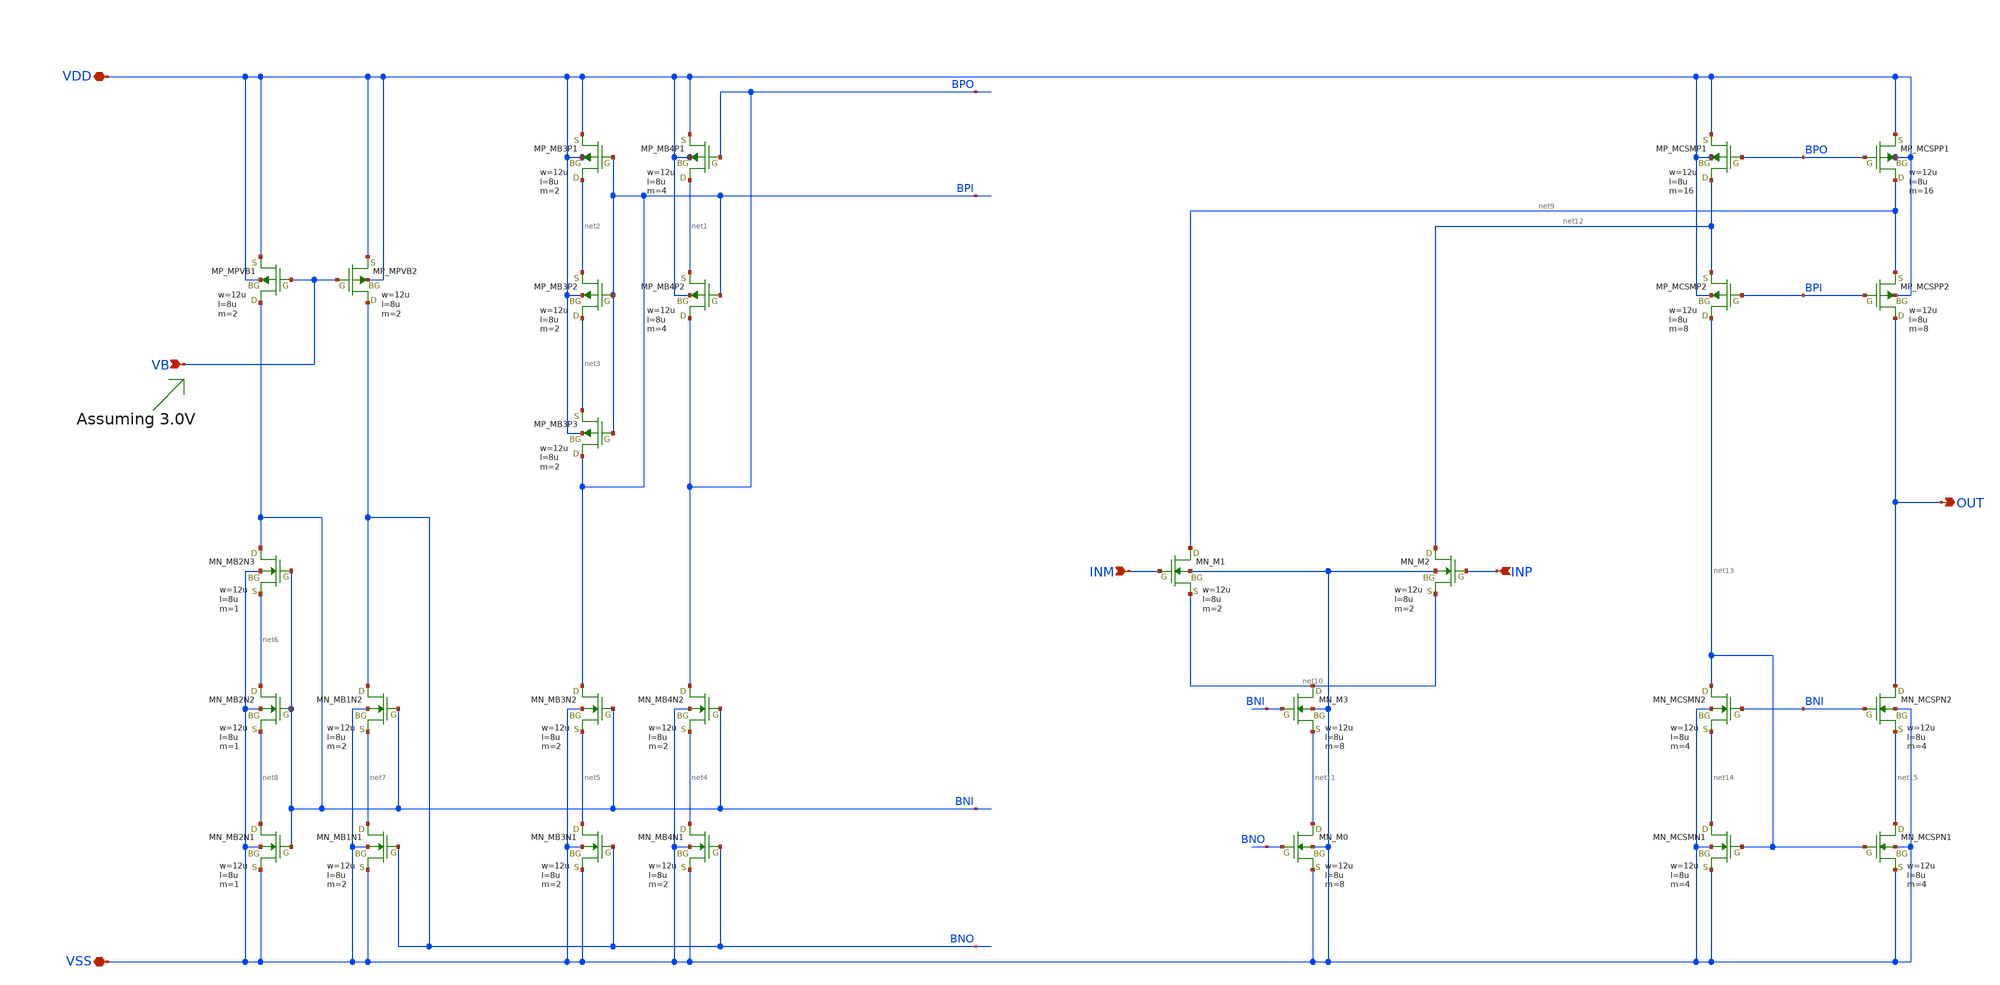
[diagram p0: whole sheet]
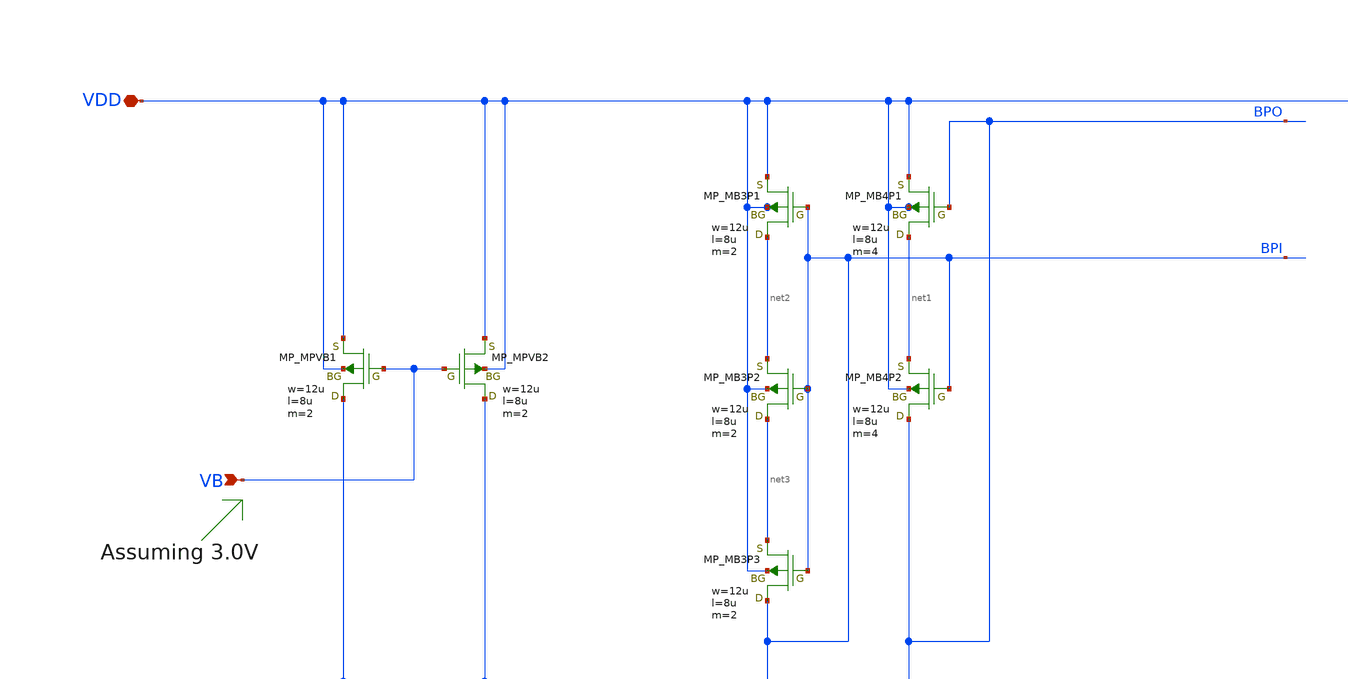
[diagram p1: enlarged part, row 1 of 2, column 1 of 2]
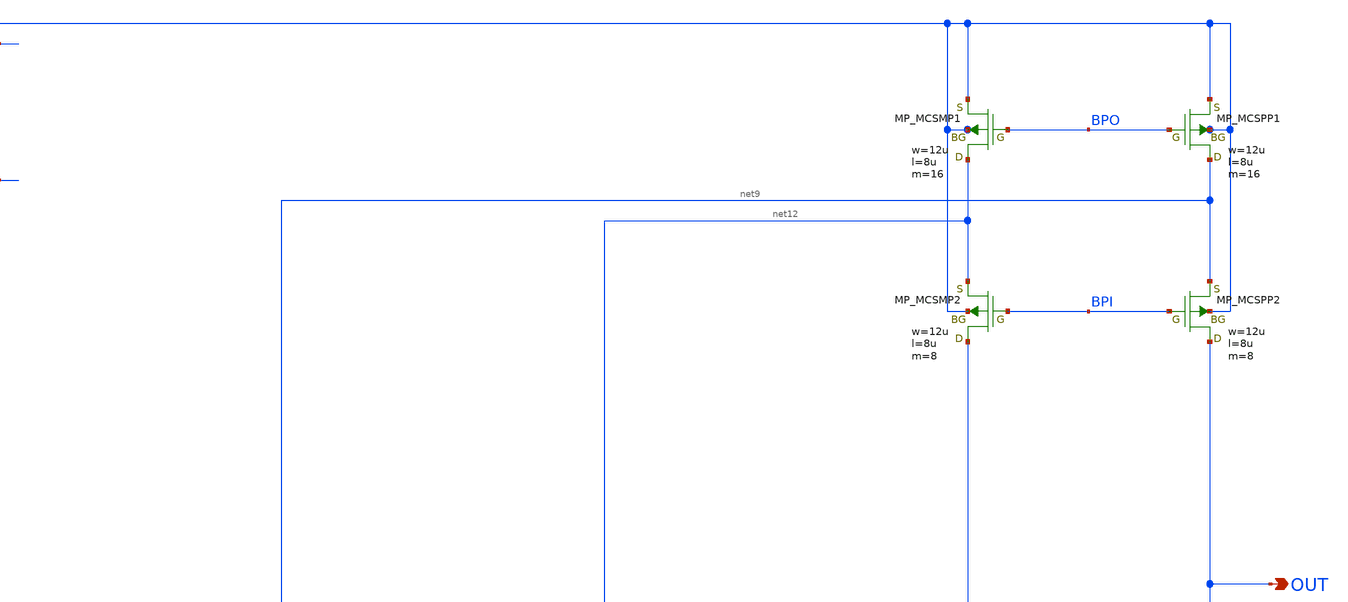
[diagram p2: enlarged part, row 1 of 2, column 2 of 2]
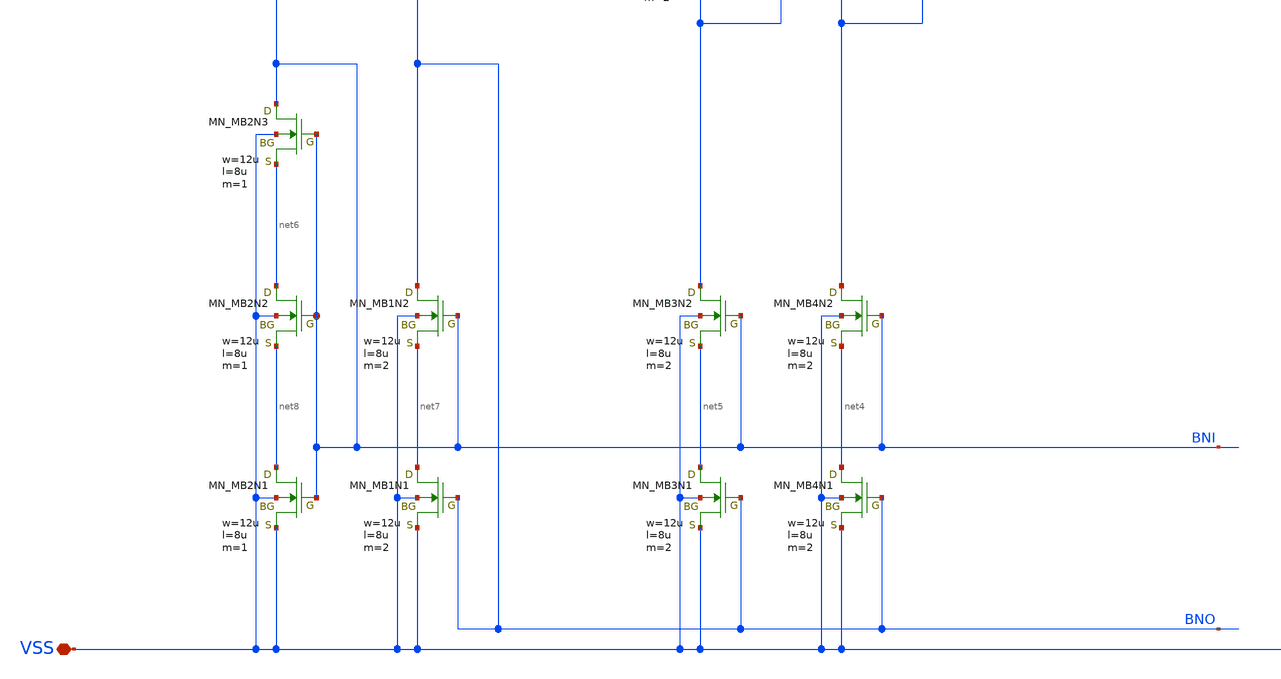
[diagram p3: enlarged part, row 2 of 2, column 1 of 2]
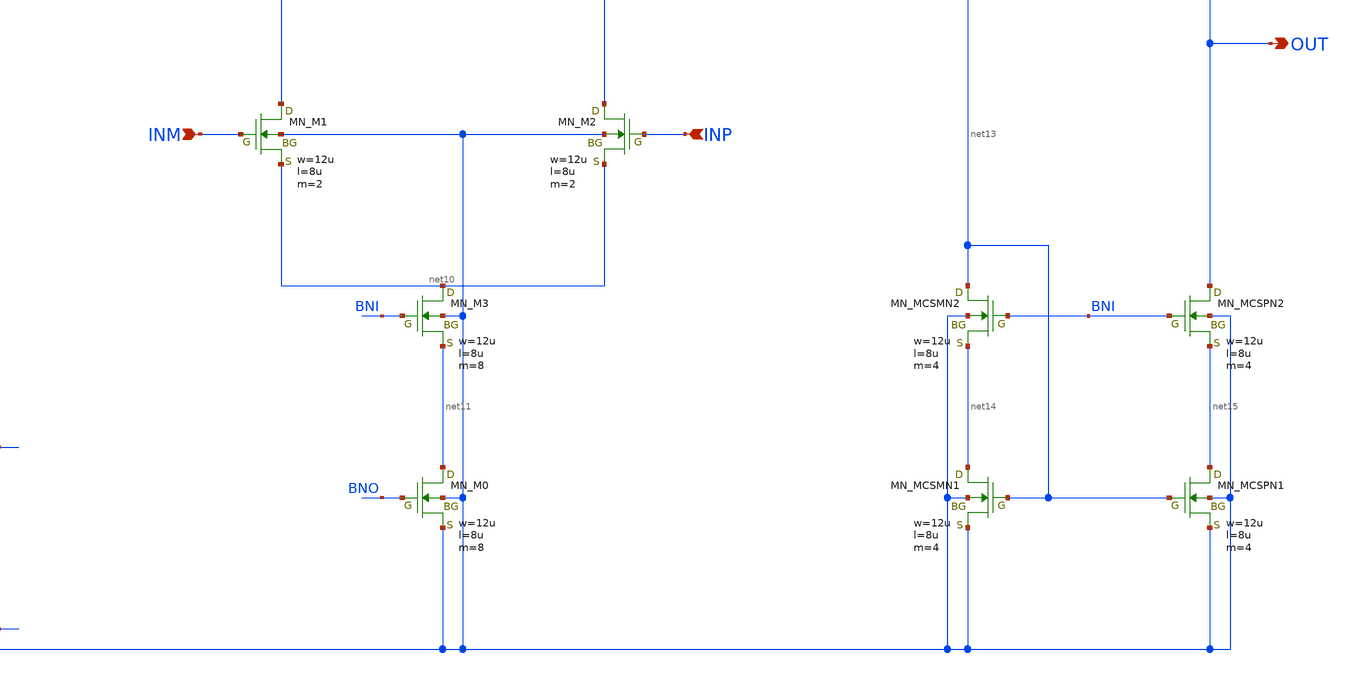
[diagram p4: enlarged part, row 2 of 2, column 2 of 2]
** sch_path: OpenSUSI-TR10/opamp_r2r/folded_1st.sch
**.subckt folded_1st VDD VSS INM INP VB OUT
*.iopin VDD
*.iopin VSS
*.ipin INM
*.ipin INP
*.ipin VB
*.opin OUT
XMB4P1 net1 BPO VDD VDD PMOS w=12u l=8u as=0 ad=0 ps=0 pd=0 nrd=0 nrs=0 m=4
XMB4P2 BPO BPI net1 VDD PMOS w=12u l=8u as=0 ad=0 ps=0 pd=0 nrd=0 nrs=0 m=4
XMB3P1 net2 BPI VDD VDD PMOS w=12u l=8u as=0 ad=0 ps=0 pd=0 nrd=0 nrs=0 m=2
XMB3P2 net3 BPI net2 VDD PMOS w=12u l=8u as=0 ad=0 ps=0 pd=0 nrd=0 nrs=0 m=2
XMB3P3 BPI BPI net3 VDD PMOS w=12u l=8u as=0 ad=0 ps=0 pd=0 nrd=0 nrs=0 m=2
XMB4N2 BPO BNI net4 VSS NMOS w=12u l=8u as=0 ad=0 ps=0 pd=0 nrd=0 nrs=0 m=2
XMB3N2 BPI BNI net5 VSS NMOS w=12u l=8u as=0 ad=0 ps=0 pd=0 nrd=0 nrs=0 m=2
XMB4N1 net4 BNO VSS VSS NMOS w=12u l=8u as=0 ad=0 ps=0 pd=0 nrd=0 nrs=0 m=2
XMB3N1 net5 BNO VSS VSS NMOS w=12u l=8u as=0 ad=0 ps=0 pd=0 nrd=0 nrs=0 m=2
XMB1N2 BNO BNI net7 VSS NMOS w=12u l=8u as=0 ad=0 ps=0 pd=0 nrd=0 nrs=0 m=2
XMB2N2 net6 BNI net8 VSS NMOS w=12u l=8u as=0 ad=0 ps=0 pd=0 nrd=0 nrs=0 m=1
XMB1N1 net7 BNO VSS VSS NMOS w=12u l=8u as=0 ad=0 ps=0 pd=0 nrd=0 nrs=0 m=2
XMB2N1 net8 BNI VSS VSS NMOS w=12u l=8u as=0 ad=0 ps=0 pd=0 nrd=0 nrs=0 m=1
XMB2N3 BNI BNI net6 VSS NMOS w=12u l=8u as=0 ad=0 ps=0 pd=0 nrd=0 nrs=0 m=1
XM3 net10 BNI net11 VSS NMOS w=12u l=8u as=0 ad=0 ps=0 pd=0 nrd=0 nrs=0 m=8
XM0 net11 BNO VSS VSS NMOS w=12u l=8u as=0 ad=0 ps=0 pd=0 nrd=0 nrs=0 m=8
XM1 net9 INM net10 VSS NMOS w=12u l=8u as=0 ad=0 ps=0 pd=0 nrd=0 nrs=0 m=2
XM2 net12 INP net10 VSS NMOS w=12u l=8u as=0 ad=0 ps=0 pd=0 nrd=0 nrs=0 m=2
XMCSMP1 net12 BPO VDD VDD PMOS w=12u l=8u as=0 ad=0 ps=0 pd=0 nrd=0 nrs=0 m=16
XMCSMP2 net13 BPI net12 VDD PMOS w=12u l=8u as=0 ad=0 ps=0 pd=0 nrd=0 nrs=0 m=8
XMCSPP1 net9 BPO VDD VDD PMOS w=12u l=8u as=0 ad=0 ps=0 pd=0 nrd=0 nrs=0 m=16
XMCSPP2 OUT BPI net9 VDD PMOS w=12u l=8u as=0 ad=0 ps=0 pd=0 nrd=0 nrs=0 m=8
XMCSMN2 net13 BNI net14 VSS NMOS w=12u l=8u as=0 ad=0 ps=0 pd=0 nrd=0 nrs=0 m=4
XMCSMN1 net14 net13 VSS VSS NMOS w=12u l=8u as=0 ad=0 ps=0 pd=0 nrd=0 nrs=0 m=4
XMCSPN2 OUT BNI net15 VSS NMOS w=12u l=8u as=0 ad=0 ps=0 pd=0 nrd=0 nrs=0 m=4
XMCSPN1 net15 net13 VSS VSS NMOS w=12u l=8u as=0 ad=0 ps=0 pd=0 nrd=0 nrs=0 m=4
XMPVB1 BNI VB VDD VDD PMOS w=12u l=8u as=0 ad=0 ps=0 pd=0 nrd=0 nrs=0 m=2
XMPVB2 BNO VB VDD VDD PMOS w=12u l=8u as=0 ad=0 ps=0 pd=0 nrd=0 nrs=0 m=2
**.ends
.end
